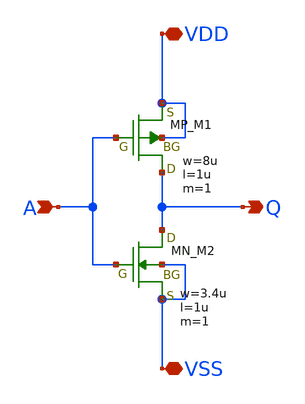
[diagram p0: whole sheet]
** sch_path: member_project/inverter/RISE-A/sai1231s/inverter_drc_rev1.sch
**.subckt inverter_drc_rev1 Q A VDD VSS
*.opin Q
*.ipin A
*.iopin VDD
*.iopin VSS
XM1 Q A VDD VDD PMOS w=8u l=1u nrd=0 nrs=0 m=1
XM2 Q A VSS VSS NMOS w=3.4u l=1u nrd=0 nrs=0 m=1
**.ends
.end
